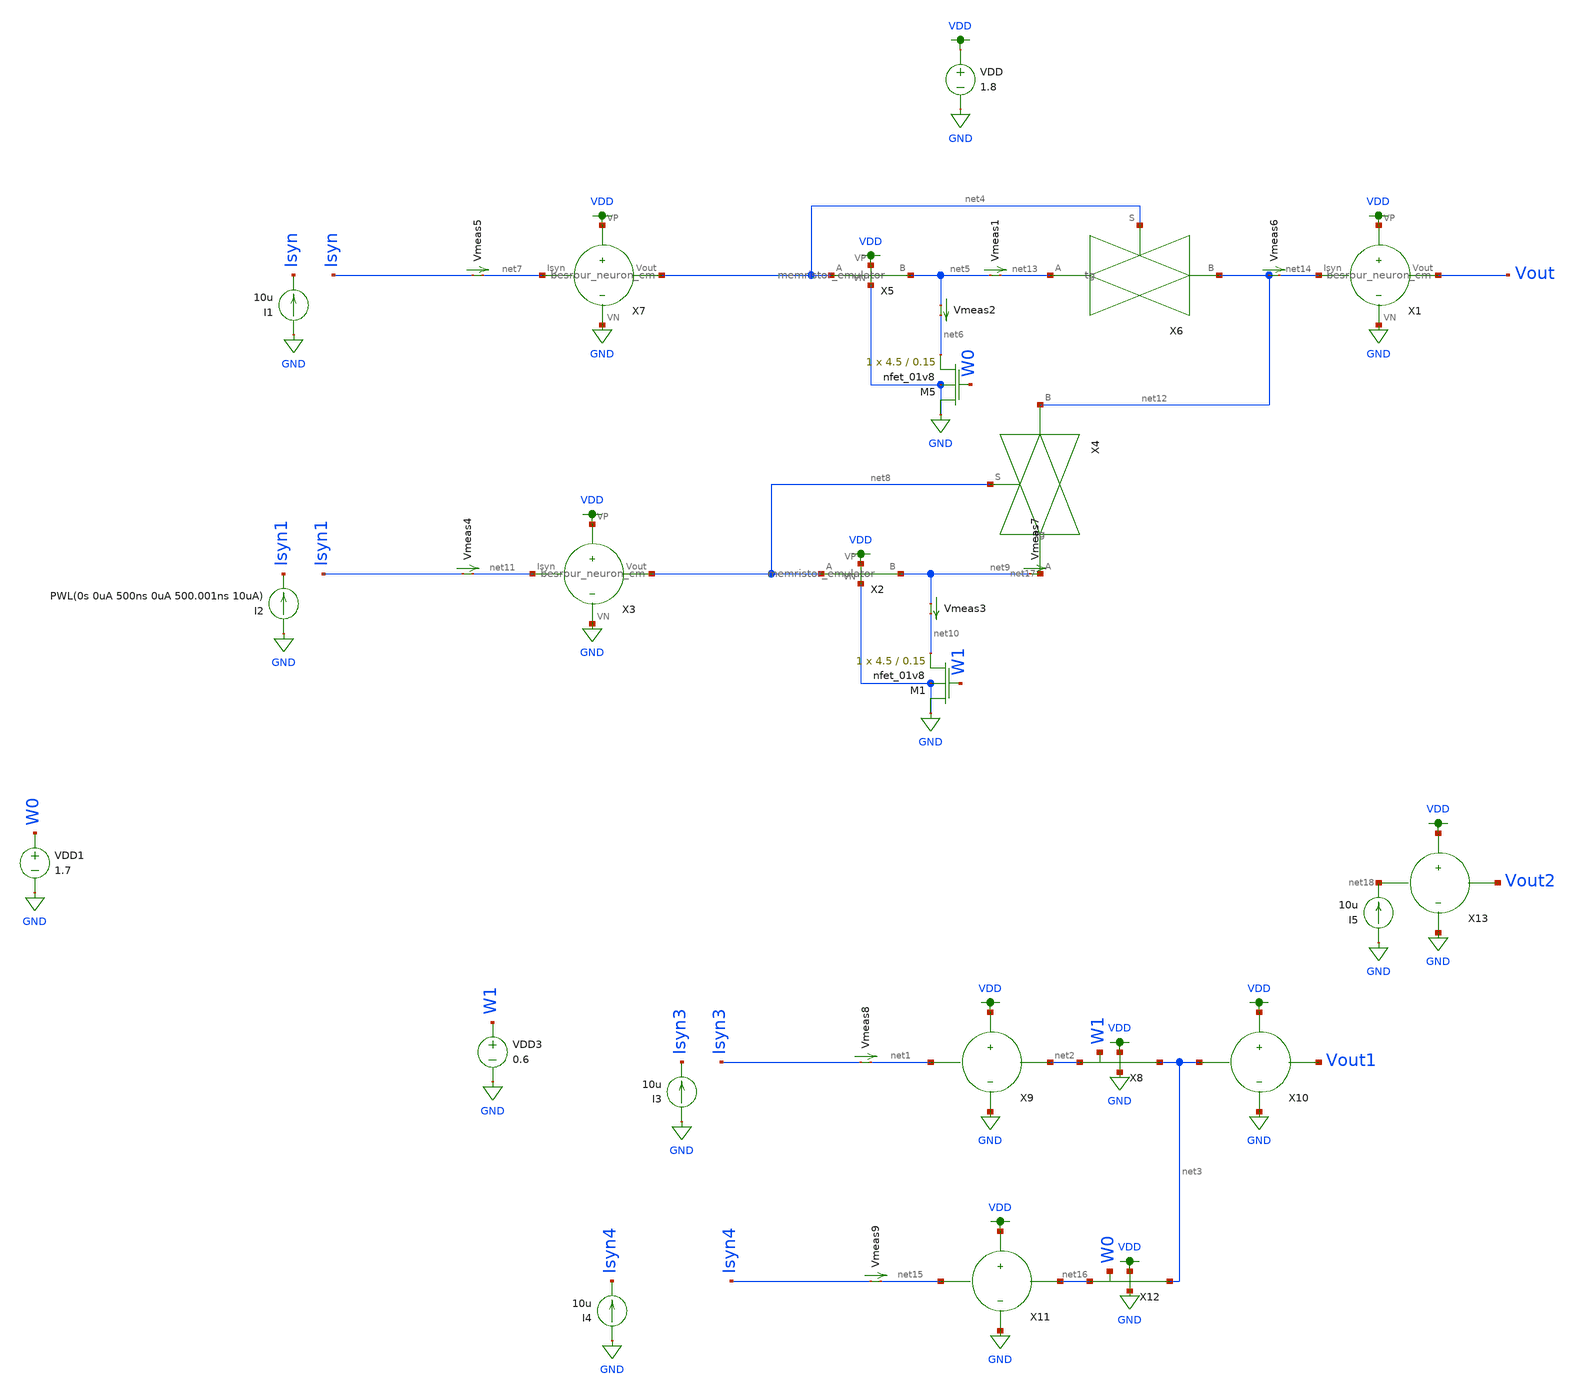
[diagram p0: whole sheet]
** sch_path: schematic/tran_besrour_mem.sch
**.subckt tran_besrour_mem
VDD VDD GND 1.8
VDD1 W0 GND 1.7
I3 GND Isyn3 10u
Vmeas8 Isyn3 net1 0
.save i(vmeas8)
I1 GND Isyn 10u
Vmeas2 net5 net6 0
.save i(vmeas2)
XM5 GND W0 net6 GND sky130_fd_pr__nfet_01v8 L=0.15 W=4.5 nf=1 ad='int((nf+1)/2) * W/nf * 0.29' as='int((nf+2)/2) * W/nf * 0.29'
+ pd='2*int((nf+1)/2) * (W/nf + 0.29)' ps='2*int((nf+2)/2) * (W/nf + 0.29)' nrd='0.29 / W' nrs='0.29 / W'
+ sa=0 sb=0 sd=0 mult=1 m=1
X5 VDD GND net5 net4 memristor_emulator
X7 net7 net4 VDD GND besrour_neuron_cm
X1 net14 Vout VDD GND besrour_neuron_cm
Vmeas1 net5 net13 0
.save i(vmeas1)
Vmeas5 Isyn net7 0
.save i(vmeas5)
I2 GND Isyn1 PWL(0s 0uA 500ns 0uA 500.001ns 10uA)
Vmeas3 net9 net10 0
.save i(vmeas3)
XM1 GND W1 net10 GND sky130_fd_pr__nfet_01v8 L=0.15 W=4.5 nf=1 ad='int((nf+1)/2) * W/nf * 0.29' as='int((nf+2)/2) * W/nf * 0.29'
+ pd='2*int((nf+1)/2) * (W/nf + 0.29)' ps='2*int((nf+2)/2) * (W/nf + 0.29)' nrd='0.29 / W' nrs='0.29 / W'
+ sa=0 sb=0 sd=0 mult=1 m=1
X2 VDD GND net9 net8 memristor_emulator
X3 net11 net8 VDD GND besrour_neuron_cm
Vmeas4 Isyn1 net11 0
.save i(vmeas4)
X4 net8 net17 net12 tg
X6 net4 net13 net12 tg
Vmeas6 net12 net14 0
.save i(vmeas6)
Vmeas7 net9 net17 0
.save i(vmeas7)
VDD3 W1 GND 0.6
X8 VDD GND net3 net2 W1 memristor_emulator_res
Vmeas9 Isyn4 net15 0
.save i(vmeas9)
X12 VDD GND net3 net16 W0 memristor_emulator_res
I4 GND Isyn4 10u
X9 net1 net2 VDD GND neuron_top
X11 net15 net16 VDD GND neuron_top
X10 net3 Vout1 VDD GND neuron_top
X13 net18 Vout2 VDD GND neuron_top
I5 GND net18 10u
**** begin user architecture code

.param W=2
.param L=0.3
.include ~/neuromorphic_computing_final/schematic/memristor_emulator_res.spice
.include ~/neuromorphic_computing_final/schematic/neuron_top.spice
.tran 0.5ns 2us
.save all


.option wnflag=1
.param MC_SWITCH=0.0
.lib ~/skywater/skywater-pdk/libraries/sky130_fd_pr_ngspice/latest/models/sky130.lib.spice tt

**** end user architecture code
**.ends

* expanding   symbol:  /home/madvlsi/neuromorphic_computing_final/schematic/memristor_emulator.sym #
*+ of pins=4
** sym_path: schematic/memristor_emulator.sym
** sch_path: schematic/memristor_emulator.sch
.subckt memristor_emulator VP VN B A
*.ipin A
*.iopin VN
*.iopin VP
*.opin B
XM1 B in_cap A B sky130_fd_pr__pfet_01v8 L=0.3 W=12 nf=1 ad='int((nf+1)/2) * W/nf * 0.29' as='int((nf+2)/2) * W/nf * 0.29'
+ pd='2*int((nf+1)/2) * (W/nf + 0.29)' ps='2*int((nf+2)/2) * (W/nf + 0.29)' nrd='0.29 / W' nrs='0.29 / W'
+ sa=0 sb=0 sd=0 mult=1 m=1
XM2 VP A in_cap VP sky130_fd_pr__pfet_01v8 L=2 W=3 nf=1 ad='int((nf+1)/2) * W/nf * 0.29' as='int((nf+2)/2) * W/nf * 0.29'
+ pd='2*int((nf+1)/2) * (W/nf + 0.29)' ps='2*int((nf+2)/2) * (W/nf + 0.29)' nrd='0.29 / W' nrs='0.29 / W'
+ sa=0 sb=0 sd=0 mult=1 m=1
XM3 VN in_cap VN VN sky130_fd_pr__nfet_01v8 L=20 W=20 nf=1 ad='int((nf+1)/2) * W/nf * 0.29' as='int((nf+2)/2) * W/nf * 0.29'
+ pd='2*int((nf+1)/2) * (W/nf + 0.29)' ps='2*int((nf+2)/2) * (W/nf + 0.29)' nrd='0.29 / W' nrs='0.29 / W'
+ sa=0 sb=0 sd=0 mult=1 m=1
XM4 VN B in_cap VN sky130_fd_pr__nfet_01v8 L=3 W=2 nf=1 ad='int((nf+1)/2) * W/nf * 0.29' as='int((nf+2)/2) * W/nf * 0.29'
+ pd='2*int((nf+1)/2) * (W/nf + 0.29)' ps='2*int((nf+2)/2) * (W/nf + 0.29)' nrd='0.29 / W' nrs='0.29 / W'
+ sa=0 sb=0 sd=0 mult=1 m=1
.ends


* expanding   symbol:  /home/madvlsi/neuromorphic_computing_final/schematic/besrour_neuron_cm.sym #
*+ of pins=4
** sym_path: schematic/besrour_neuron_cm.sym
** sch_path: schematic/besrour_neuron_cm.sch
.subckt besrour_neuron_cm Isyn Vout VP VN
*.iopin VP
*.iopin VN
*.iopin Isyn
*.opin Vout
XM2 VMEMINT net1 VP VDD sky130_fd_pr__pfet_01v8 L={L} W={W} nf=1 ad='int((nf+1)/2) * W/nf * 0.29' as='int((nf+2)/2) * W/nf * 0.29'
+ pd='2*int((nf+1)/2) * (W/nf + 0.29)' ps='2*int((nf+2)/2) * (W/nf + 0.29)' nrd='0.29 / W' nrs='0.29 / W'
+ sa=0 sb=0 sd=0 mult=1 m=1
XM3 VP net3 VMEMINT VDD sky130_fd_pr__pfet_01v8 L={L} W={W} nf=1 ad='int((nf+1)/2) * W/nf * 0.29' as='int((nf+2)/2) * W/nf * 0.29'
+ pd='2*int((nf+1)/2) * (W/nf + 0.29)' ps='2*int((nf+2)/2) * (W/nf + 0.29)' nrd='0.29 / W' nrs='0.29 / W'
+ sa=0 sb=0 sd=0 mult=1 m=1
XM4 net3 VMEMINT VP VDD sky130_fd_pr__pfet_01v8 L={L} W={W} nf=1 ad='int((nf+1)/2) * W/nf * 0.29' as='int((nf+2)/2) * W/nf * 0.29'
+ pd='2*int((nf+1)/2) * (W/nf + 0.29)' ps='2*int((nf+2)/2) * (W/nf + 0.29)' nrd='0.29 / W' nrs='0.29 / W'
+ sa=0 sb=0 sd=0 mult=1 m=1
XM5 net2 net3 VP VDD sky130_fd_pr__pfet_01v8 L={L} W={W} nf=1 ad='int((nf+1)/2) * W/nf * 0.29' as='int((nf+2)/2) * W/nf * 0.29'
+ pd='2*int((nf+1)/2) * (W/nf + 0.29)' ps='2*int((nf+2)/2) * (W/nf + 0.29)' nrd='0.29 / W' nrs='0.29 / W'
+ sa=0 sb=0 sd=0 mult=1 m=1
XM6 net3 VMEMINT VN GND sky130_fd_pr__nfet_01v8 L={L} W={W} nf=1 ad='int((nf+1)/2) * W/nf * 0.29' as='int((nf+2)/2) * W/nf * 0.29'
+ pd='2*int((nf+1)/2) * (W/nf + 0.29)' ps='2*int((nf+2)/2) * (W/nf + 0.29)' nrd='0.29 / W' nrs='0.29 / W'
+ sa=0 sb=0 sd=0 mult=1 m=1
XM8 net2 net3 VN GND sky130_fd_pr__nfet_01v8 L={L} W={W} nf=1 ad='int((nf+1)/2) * W/nf * 0.29' as='int((nf+2)/2) * W/nf * 0.29'
+ pd='2*int((nf+1)/2) * (W/nf + 0.29)' ps='2*int((nf+2)/2) * (W/nf + 0.29)' nrd='0.29 / W' nrs='0.29 / W'
+ sa=0 sb=0 sd=0 mult=1 m=1
XM9 net4 net2 VP VDD sky130_fd_pr__pfet_01v8 L={L} W={W} nf=1 ad='int((nf+1)/2) * W/nf * 0.29' as='int((nf+2)/2) * W/nf * 0.29'
+ pd='2*int((nf+1)/2) * (W/nf + 0.29)' ps='2*int((nf+2)/2) * (W/nf + 0.29)' nrd='0.29 / W' nrs='0.29 / W'
+ sa=0 sb=0 sd=0 mult=1 m=1
XM10 net4 net2 VN GND sky130_fd_pr__nfet_01v8 L={L} W={W} nf=1 ad='int((nf+1)/2) * W/nf * 0.29' as='int((nf+2)/2) * W/nf * 0.29'
+ pd='2*int((nf+1)/2) * (W/nf + 0.29)' ps='2*int((nf+2)/2) * (W/nf + 0.29)' nrd='0.29 / W' nrs='0.29 / W'
+ sa=0 sb=0 sd=0 mult=1 m=1
XM11 Vout net4 VP VDD sky130_fd_pr__pfet_01v8 L={L} W={W} nf=1 ad='int((nf+1)/2) * W/nf * 0.29' as='int((nf+2)/2) * W/nf * 0.29'
+ pd='2*int((nf+1)/2) * (W/nf + 0.29)' ps='2*int((nf+2)/2) * (W/nf + 0.29)' nrd='0.29 / W' nrs='0.29 / W'
+ sa=0 sb=0 sd=0 mult=1 m=1
XM12 Vout net4 VN GND sky130_fd_pr__nfet_01v8 L={L} W={W} nf=1 ad='int((nf+1)/2) * W/nf * 0.29' as='int((nf+2)/2) * W/nf * 0.29'
+ pd='2*int((nf+1)/2) * (W/nf + 0.29)' ps='2*int((nf+2)/2) * (W/nf + 0.29)' nrd='0.29 / W' nrs='0.29 / W'
+ sa=0 sb=0 sd=0 mult=1 m=1
XM13 net1 Isyn VN GND sky130_fd_pr__nfet_01v8 L={L} W={W} nf=1 ad='int((nf+1)/2) * W/nf * 0.29' as='int((nf+2)/2) * W/nf * 0.29'
+ pd='2*int((nf+1)/2) * (W/nf + 0.29)' ps='2*int((nf+2)/2) * (W/nf + 0.29)' nrd='0.29 / W' nrs='0.29 / W'
+ sa=0 sb=0 sd=0 mult=1 m=1
XM14 VN Isyn Isyn GND sky130_fd_pr__nfet_01v8 L={L} W={W} nf=1 ad='int((nf+1)/2) * W/nf * 0.29' as='int((nf+2)/2) * W/nf * 0.29'
+ pd='2*int((nf+1)/2) * (W/nf + 0.29)' ps='2*int((nf+2)/2) * (W/nf + 0.29)' nrd='0.29 / W' nrs='0.29 / W'
+ sa=0 sb=0 sd=0 mult=1 m=1
XM1 VP net1 net1 VDD sky130_fd_pr__pfet_01v8 L={L} W={W} nf=1 ad='int((nf+1)/2) * W/nf * 0.29' as='int((nf+2)/2) * W/nf * 0.29'
+ pd='2*int((nf+1)/2) * (W/nf + 0.29)' ps='2*int((nf+2)/2) * (W/nf + 0.29)' nrd='0.29 / W' nrs='0.29 / W'
+ sa=0 sb=0 sd=0 mult=1 m=1
XM7 VN net2 VMEMINT GND sky130_fd_pr__nfet_01v8 L={L} W={W} nf=1 ad='int((nf+1)/2) * W/nf * 0.29' as='int((nf+2)/2) * W/nf * 0.29'
+ pd='2*int((nf+1)/2) * (W/nf + 0.29)' ps='2*int((nf+2)/2) * (W/nf + 0.29)' nrd='0.29 / W' nrs='0.29 / W'
+ sa=0 sb=0 sd=0 mult=1 m=1
XC1 VMEMINT VN sky130_fd_pr__cap_mim_m3_1 W=9.3 L=14 MF=1 m=1
XC2 net2 VN sky130_fd_pr__cap_mim_m3_1 W=9.3 L=14 MF=1 m=1
.ends


* expanding   symbol:  /home/madvlsi/neuromorphic_computing_final/schematic/tg.sym # of pins=3
** sym_path: schematic/tg.sym
** sch_path: schematic/tg.sch
.subckt tg S A B
*.ipin S
*.iopin B
*.iopin A
X1 S GND VDD net1 inverter
XM1 B net1 A VDD sky130_fd_pr__pfet_01v8 L=0.3 W=6 nf=1 ad='int((nf+1)/2) * W/nf * 0.29' as='int((nf+2)/2) * W/nf * 0.29'
+ pd='2*int((nf+1)/2) * (W/nf + 0.29)' ps='2*int((nf+2)/2) * (W/nf + 0.29)' nrd='0.29 / W' nrs='0.29 / W'
+ sa=0 sb=0 sd=0 mult=1 m=1
XM2 B S A GND sky130_fd_pr__nfet_01v8 L=0.3 W=6 nf=1 ad='int((nf+1)/2) * W/nf * 0.29' as='int((nf+2)/2) * W/nf * 0.29'
+ pd='2*int((nf+1)/2) * (W/nf + 0.29)' ps='2*int((nf+2)/2) * (W/nf + 0.29)' nrd='0.29 / W' nrs='0.29 / W'
+ sa=0 sb=0 sd=0 mult=1 m=1
.ends


* expanding   symbol:  /home/madvlsi/neuromorphic_computing_final/schematic/inverter.sym # of pins=4
** sym_path: schematic/inverter.sym
** sch_path: schematic/inverter.sch
.subckt inverter A VN VP Y
*.ipin A
*.iopin VP
*.iopin VN
*.opin Y
XM1 Y A VN VN sky130_fd_pr__nfet_01v8 L=0.15 W=1 nf=1 ad='int((nf+1)/2) * W/nf * 0.29' as='int((nf+2)/2) * W/nf * 0.29'
+ pd='2*int((nf+1)/2) * (W/nf + 0.29)' ps='2*int((nf+2)/2) * (W/nf + 0.29)' nrd='0.29 / W' nrs='0.29 / W'
+ sa=0 sb=0 sd=0 mult=1 m=1
XM2 Y A VP VP sky130_fd_pr__pfet_01v8 L=0.15 W=1 nf=1 ad='int((nf+1)/2) * W/nf * 0.29' as='int((nf+2)/2) * W/nf * 0.29'
+ pd='2*int((nf+1)/2) * (W/nf + 0.29)' ps='2*int((nf+2)/2) * (W/nf + 0.29)' nrd='0.29 / W' nrs='0.29 / W'
+ sa=0 sb=0 sd=0 mult=1 m=1
.ends

.GLOBAL GND
.GLOBAL VDD
.end
